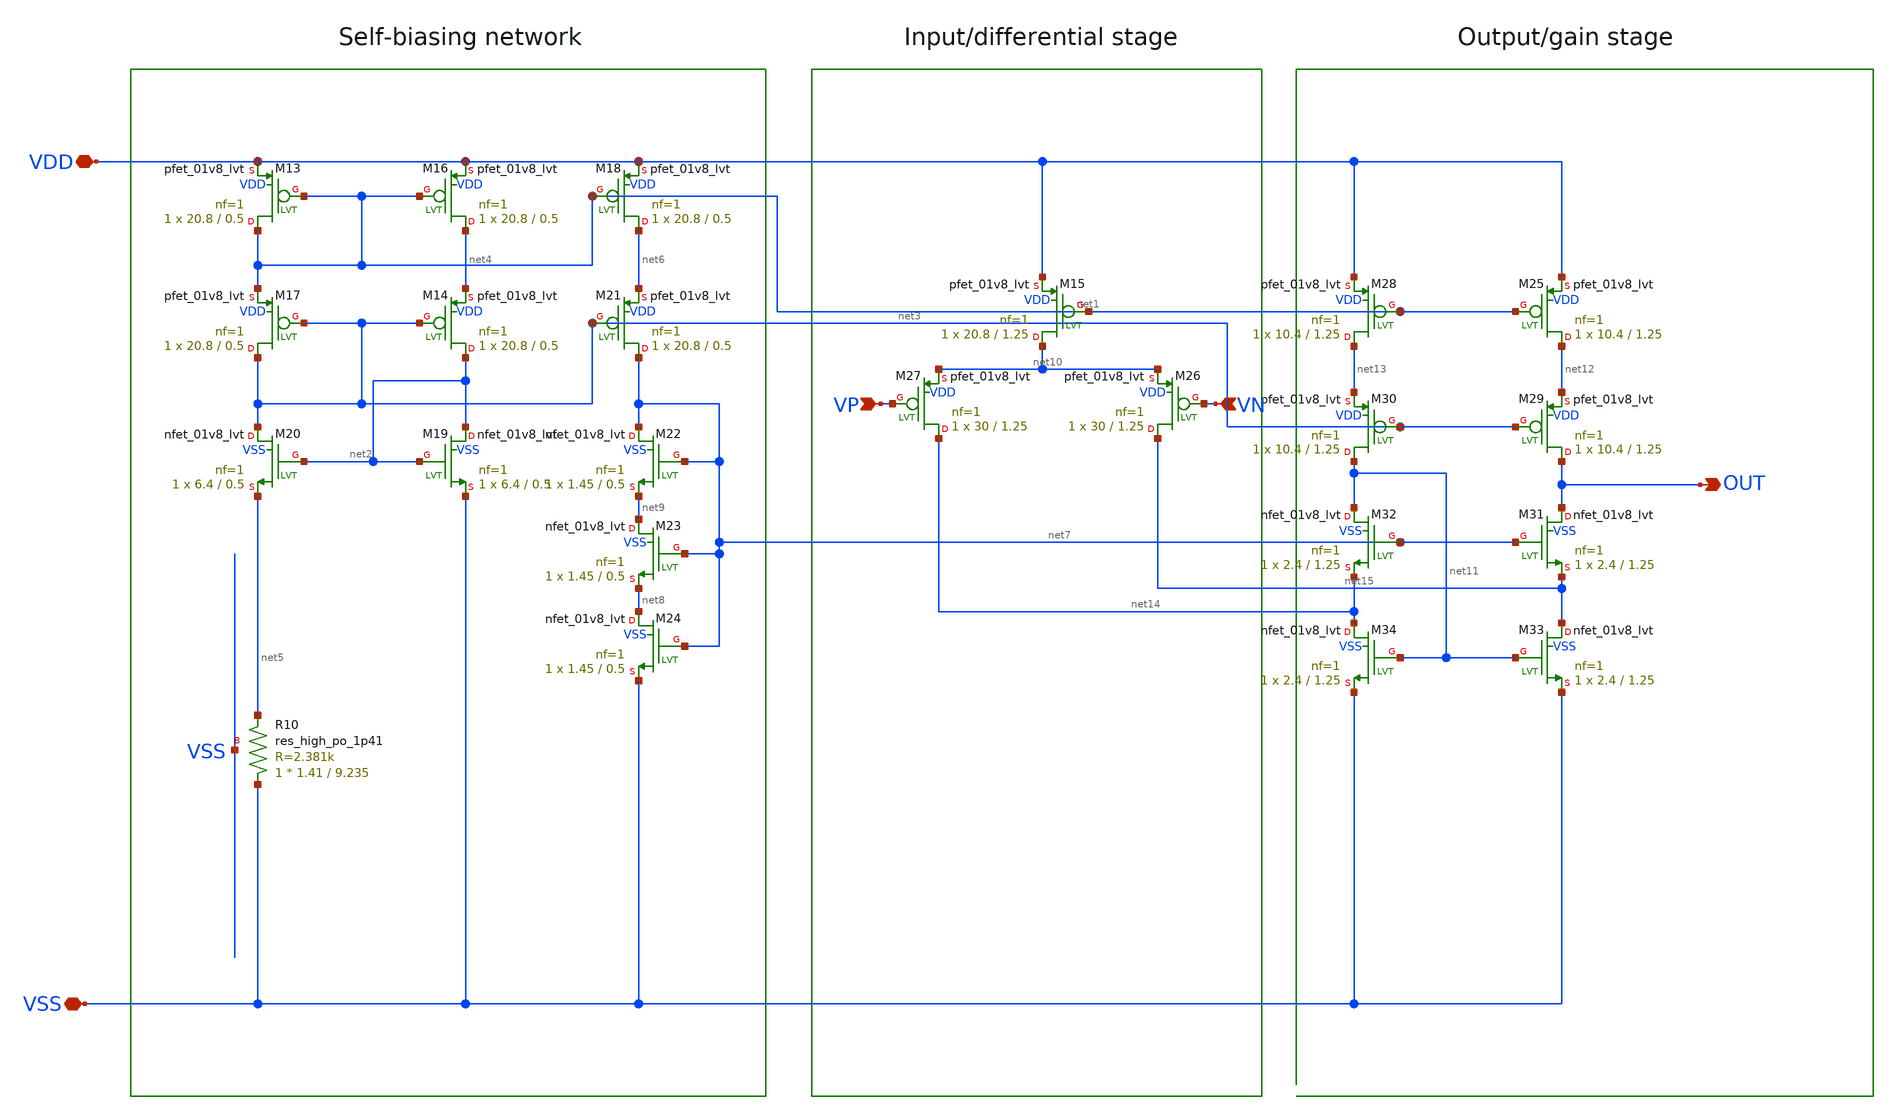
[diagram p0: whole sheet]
** sch_path: bandgap/bgr/bgr-opamp2.sch
**.subckt bgr-opamp2 VSS VDD VP VN OUT
*.iopin VSS
*.iopin VDD
*.ipin VP
*.ipin VN
*.opin OUT
XR10 VSS net5 VSS sky130_fd_pr__res_high_po_1p41 L=9.235 mult=1 m=1
XM19 net2 net2 VSS VSS sky130_fd_pr__nfet_01v8_lvt L=0.5 W=6.4 nf=1 ad='int((nf+1)/2) * W/nf * 0.29'
+ as='int((nf+2)/2) * W/nf * 0.29' pd='2*int((nf+1)/2) * (W/nf + 0.29)' ps='2*int((nf+2)/2) * (W/nf + 0.29)'
+ nrd='0.29 / W' nrs='0.29 / W' sa=0 sb=0 sd=0 mult=1 m=1
XM20 net3 net2 net5 VSS sky130_fd_pr__nfet_01v8_lvt L=0.5 W=6.4 nf=1 ad='int((nf+1)/2) * W/nf * 0.29'
+ as='int((nf+2)/2) * W/nf * 0.29' pd='2*int((nf+1)/2) * (W/nf + 0.29)' ps='2*int((nf+2)/2) * (W/nf + 0.29)'
+ nrd='0.29 / W' nrs='0.29 / W' sa=0 sb=0 sd=0 mult=1 m=1
XM16 net4 net1 VDD VDD sky130_fd_pr__pfet_01v8_lvt L=0.5 W=20.8 nf=1 ad='int((nf+1)/2) * W/nf * 0.29'
+ as='int((nf+2)/2) * W/nf * 0.29' pd='2*int((nf+1)/2) * (W/nf + 0.29)' ps='2*int((nf+2)/2) * (W/nf + 0.29)'
+ nrd='0.29 / W' nrs='0.29 / W' sa=0 sb=0 sd=0 mult=1 m=1
XM13 net1 net1 VDD VDD sky130_fd_pr__pfet_01v8_lvt L=0.5 W=20.8 nf=1 ad='int((nf+1)/2) * W/nf * 0.29'
+ as='int((nf+2)/2) * W/nf * 0.29' pd='2*int((nf+1)/2) * (W/nf + 0.29)' ps='2*int((nf+2)/2) * (W/nf + 0.29)'
+ nrd='0.29 / W' nrs='0.29 / W' sa=0 sb=0 sd=0 mult=1 m=1
XM14 net2 net3 net4 VDD sky130_fd_pr__pfet_01v8_lvt L=0.5 W=20.8 nf=1 ad='int((nf+1)/2) * W/nf * 0.29'
+ as='int((nf+2)/2) * W/nf * 0.29' pd='2*int((nf+1)/2) * (W/nf + 0.29)' ps='2*int((nf+2)/2) * (W/nf + 0.29)'
+ nrd='0.29 / W' nrs='0.29 / W' sa=0 sb=0 sd=0 mult=1 m=1
XM17 net3 net3 net1 VDD sky130_fd_pr__pfet_01v8_lvt L=0.5 W=20.8 nf=1 ad='int((nf+1)/2) * W/nf * 0.29'
+ as='int((nf+2)/2) * W/nf * 0.29' pd='2*int((nf+1)/2) * (W/nf + 0.29)' ps='2*int((nf+2)/2) * (W/nf + 0.29)'
+ nrd='0.29 / W' nrs='0.29 / W' sa=0 sb=0 sd=0 mult=1 m=1
XM18 net6 net1 VDD VDD sky130_fd_pr__pfet_01v8_lvt L=0.5 W=20.8 nf=1 ad='int((nf+1)/2) * W/nf * 0.29'
+ as='int((nf+2)/2) * W/nf * 0.29' pd='2*int((nf+1)/2) * (W/nf + 0.29)' ps='2*int((nf+2)/2) * (W/nf + 0.29)'
+ nrd='0.29 / W' nrs='0.29 / W' sa=0 sb=0 sd=0 mult=1 m=1
XM21 net7 net3 net6 VDD sky130_fd_pr__pfet_01v8_lvt L=0.5 W=20.8 nf=1 ad='int((nf+1)/2) * W/nf * 0.29'
+ as='int((nf+2)/2) * W/nf * 0.29' pd='2*int((nf+1)/2) * (W/nf + 0.29)' ps='2*int((nf+2)/2) * (W/nf + 0.29)'
+ nrd='0.29 / W' nrs='0.29 / W' sa=0 sb=0 sd=0 mult=1 m=1
XM22 net7 net7 net9 VSS sky130_fd_pr__nfet_01v8_lvt L=0.5 W=1.45 nf=1 ad='int((nf+1)/2) * W/nf * 0.29'
+ as='int((nf+2)/2) * W/nf * 0.29' pd='2*int((nf+1)/2) * (W/nf + 0.29)' ps='2*int((nf+2)/2) * (W/nf + 0.29)'
+ nrd='0.29 / W' nrs='0.29 / W' sa=0 sb=0 sd=0 mult=1 m=1
XM23 net9 net7 net8 VSS sky130_fd_pr__nfet_01v8_lvt L=0.5 W=1.45 nf=1 ad='int((nf+1)/2) * W/nf * 0.29'
+ as='int((nf+2)/2) * W/nf * 0.29' pd='2*int((nf+1)/2) * (W/nf + 0.29)' ps='2*int((nf+2)/2) * (W/nf + 0.29)'
+ nrd='0.29 / W' nrs='0.29 / W' sa=0 sb=0 sd=0 mult=1 m=1
XM24 net8 net7 VSS VSS sky130_fd_pr__nfet_01v8_lvt L=0.5 W=1.45 nf=1 ad='int((nf+1)/2) * W/nf * 0.29'
+ as='int((nf+2)/2) * W/nf * 0.29' pd='2*int((nf+1)/2) * (W/nf + 0.29)' ps='2*int((nf+2)/2) * (W/nf + 0.29)'
+ nrd='0.29 / W' nrs='0.29 / W' sa=0 sb=0 sd=0 mult=1 m=1
XM26 net15 VN net10 VDD sky130_fd_pr__pfet_01v8_lvt L=1.25 W=30 nf=1 ad='int((nf+1)/2) * W/nf * 0.29'
+ as='int((nf+2)/2) * W/nf * 0.29' pd='2*int((nf+1)/2) * (W/nf + 0.29)' ps='2*int((nf+2)/2) * (W/nf + 0.29)'
+ nrd='0.29 / W' nrs='0.29 / W' sa=0 sb=0 sd=0 mult=1 m=1
XM27 net14 VP net10 VDD sky130_fd_pr__pfet_01v8_lvt L=1.25 W=30 nf=1 ad='int((nf+1)/2) * W/nf * 0.29'
+ as='int((nf+2)/2) * W/nf * 0.29' pd='2*int((nf+1)/2) * (W/nf + 0.29)' ps='2*int((nf+2)/2) * (W/nf + 0.29)'
+ nrd='0.29 / W' nrs='0.29 / W' sa=0 sb=0 sd=0 mult=1 m=1
XM15 net10 net1 VDD VDD sky130_fd_pr__pfet_01v8_lvt L=1.25 W=20.8 nf=1 ad='int((nf+1)/2) * W/nf * 0.29'
+ as='int((nf+2)/2) * W/nf * 0.29' pd='2*int((nf+1)/2) * (W/nf + 0.29)' ps='2*int((nf+2)/2) * (W/nf + 0.29)'
+ nrd='0.29 / W' nrs='0.29 / W' sa=0 sb=0 sd=0 mult=1 m=1
XM25 net12 net1 VDD VDD sky130_fd_pr__pfet_01v8_lvt L=1.25 W=10.4 nf=1 ad='int((nf+1)/2) * W/nf * 0.29'
+ as='int((nf+2)/2) * W/nf * 0.29' pd='2*int((nf+1)/2) * (W/nf + 0.29)' ps='2*int((nf+2)/2) * (W/nf + 0.29)'
+ nrd='0.29 / W' nrs='0.29 / W' sa=0 sb=0 sd=0 mult=1 m=1
XM28 net13 net1 VDD VDD sky130_fd_pr__pfet_01v8_lvt L=1.25 W=10.4 nf=1 ad='int((nf+1)/2) * W/nf * 0.29'
+ as='int((nf+2)/2) * W/nf * 0.29' pd='2*int((nf+1)/2) * (W/nf + 0.29)' ps='2*int((nf+2)/2) * (W/nf + 0.29)'
+ nrd='0.29 / W' nrs='0.29 / W' sa=0 sb=0 sd=0 mult=1 m=1
XM29 OUT net3 net12 VDD sky130_fd_pr__pfet_01v8_lvt L=1.25 W=10.4 nf=1 ad='int((nf+1)/2) * W/nf * 0.29'
+ as='int((nf+2)/2) * W/nf * 0.29' pd='2*int((nf+1)/2) * (W/nf + 0.29)' ps='2*int((nf+2)/2) * (W/nf + 0.29)'
+ nrd='0.29 / W' nrs='0.29 / W' sa=0 sb=0 sd=0 mult=1 m=1
XM30 net11 net3 net13 VDD sky130_fd_pr__pfet_01v8_lvt L=1.25 W=10.4 nf=1 ad='int((nf+1)/2) * W/nf * 0.29'
+ as='int((nf+2)/2) * W/nf * 0.29' pd='2*int((nf+1)/2) * (W/nf + 0.29)' ps='2*int((nf+2)/2) * (W/nf + 0.29)'
+ nrd='0.29 / W' nrs='0.29 / W' sa=0 sb=0 sd=0 mult=1 m=1
XM31 OUT net7 net15 VSS sky130_fd_pr__nfet_01v8_lvt L=1.25 W=2.4 nf=1 ad='int((nf+1)/2) * W/nf * 0.29'
+ as='int((nf+2)/2) * W/nf * 0.29' pd='2*int((nf+1)/2) * (W/nf + 0.29)' ps='2*int((nf+2)/2) * (W/nf + 0.29)'
+ nrd='0.29 / W' nrs='0.29 / W' sa=0 sb=0 sd=0 mult=1 m=1
XM32 net11 net7 net14 VSS sky130_fd_pr__nfet_01v8_lvt L=1.25 W=2.4 nf=1 ad='int((nf+1)/2) * W/nf * 0.29'
+ as='int((nf+2)/2) * W/nf * 0.29' pd='2*int((nf+1)/2) * (W/nf + 0.29)' ps='2*int((nf+2)/2) * (W/nf + 0.29)'
+ nrd='0.29 / W' nrs='0.29 / W' sa=0 sb=0 sd=0 mult=1 m=1
XM33 net15 net11 VSS VSS sky130_fd_pr__nfet_01v8_lvt L=1.25 W=2.4 nf=1 ad='int((nf+1)/2) * W/nf * 0.29'
+ as='int((nf+2)/2) * W/nf * 0.29' pd='2*int((nf+1)/2) * (W/nf + 0.29)' ps='2*int((nf+2)/2) * (W/nf + 0.29)'
+ nrd='0.29 / W' nrs='0.29 / W' sa=0 sb=0 sd=0 mult=1 m=1
XM34 net14 net11 VSS VSS sky130_fd_pr__nfet_01v8_lvt L=1.25 W=2.4 nf=1 ad='int((nf+1)/2) * W/nf * 0.29'
+ as='int((nf+2)/2) * W/nf * 0.29' pd='2*int((nf+1)/2) * (W/nf + 0.29)' ps='2*int((nf+2)/2) * (W/nf + 0.29)'
+ nrd='0.29 / W' nrs='0.29 / W' sa=0 sb=0 sd=0 mult=1 m=1
**.ends
.end
